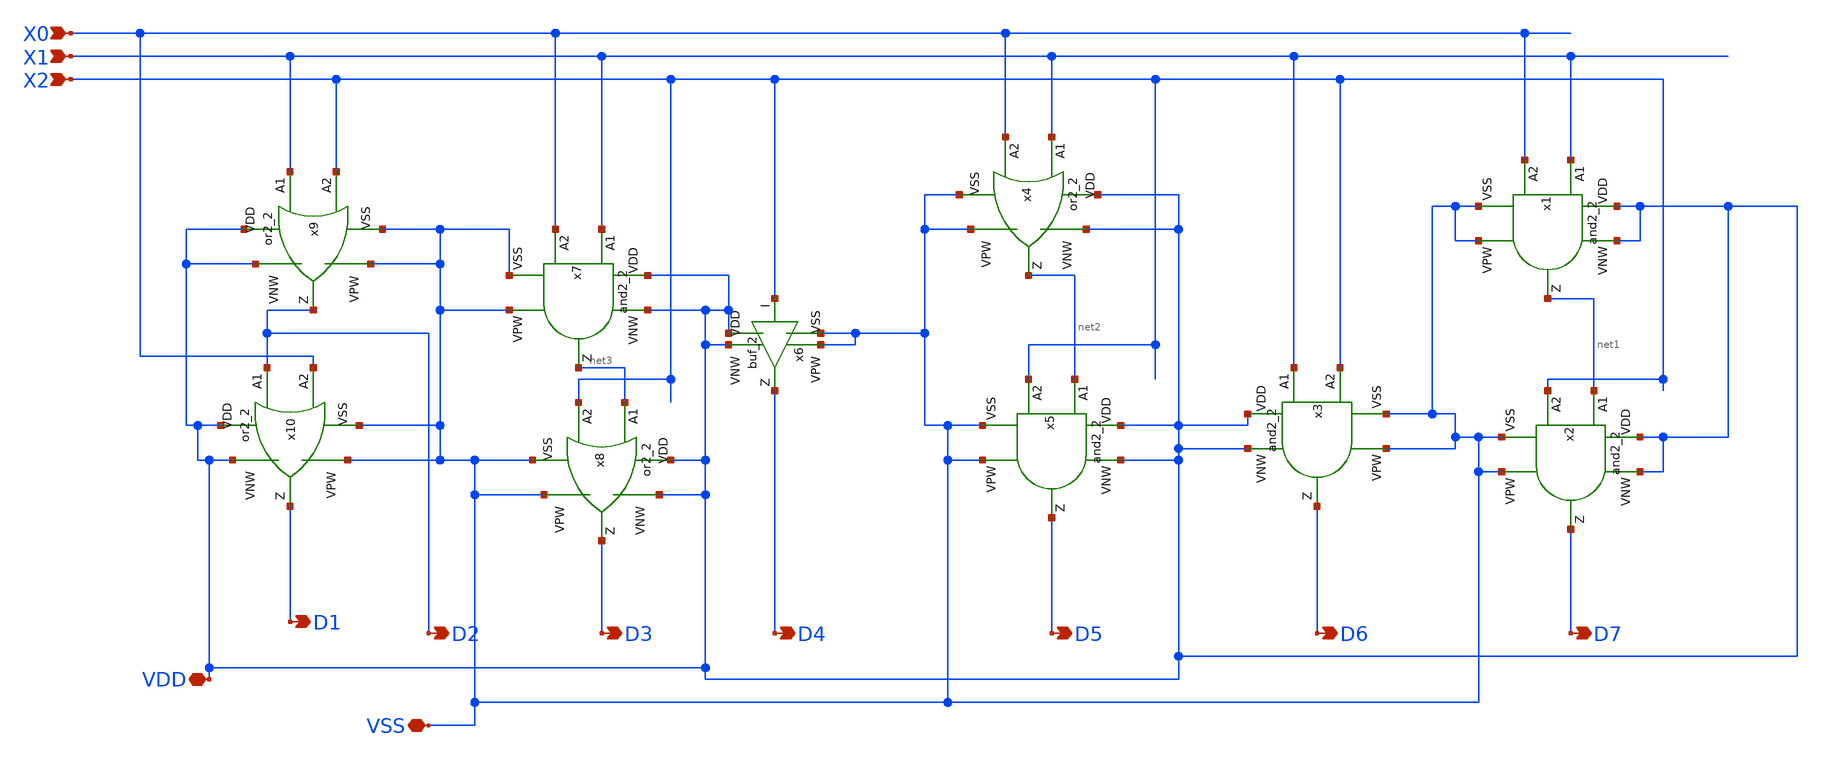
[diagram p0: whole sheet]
** sch_path: xschem/thermo_decoder.sch
**.subckt thermo_decoder X0 X1 X2 D1 D2 D3 D4 D5 D6 D7 VDD VSS
*.ipin X0
*.ipin X1
*.ipin X2
*.opin D1
*.opin D2
*.opin D3
*.opin D4
*.opin D5
*.opin D6
*.opin D7
*.iopin VDD
*.iopin VSS
x3 X1 X2 D6 VDD VDD VSS VSS gf180mcu_fd_sc_mcu7t5v0__and2_2
x4 X1 X0 net2 VDD VDD VSS VSS gf180mcu_fd_sc_mcu7t5v0__or2_2
x5 net2 X2 D5 VDD VDD VSS VSS gf180mcu_fd_sc_mcu7t5v0__and2_2
x6 X2 D4 VDD VDD VSS VSS gf180mcu_fd_sc_mcu7t5v0__buf_2
x7 X1 X0 net3 VDD VDD VSS VSS gf180mcu_fd_sc_mcu7t5v0__and2_2
x8 net3 X2 D3 VDD VDD VSS VSS gf180mcu_fd_sc_mcu7t5v0__or2_2
x9 X1 X2 D2 VDD VDD VSS VSS gf180mcu_fd_sc_mcu7t5v0__or2_2
x10 D2 X0 D1 VDD VDD VSS VSS gf180mcu_fd_sc_mcu7t5v0__or2_2
x1 X1 X0 net1 VDD VDD VSS VSS gf180mcu_fd_sc_mcu7t5v0__and2_2
x2 net1 X2 D7 VDD VDD VSS VSS gf180mcu_fd_sc_mcu7t5v0__and2_2
**.ends
.end
